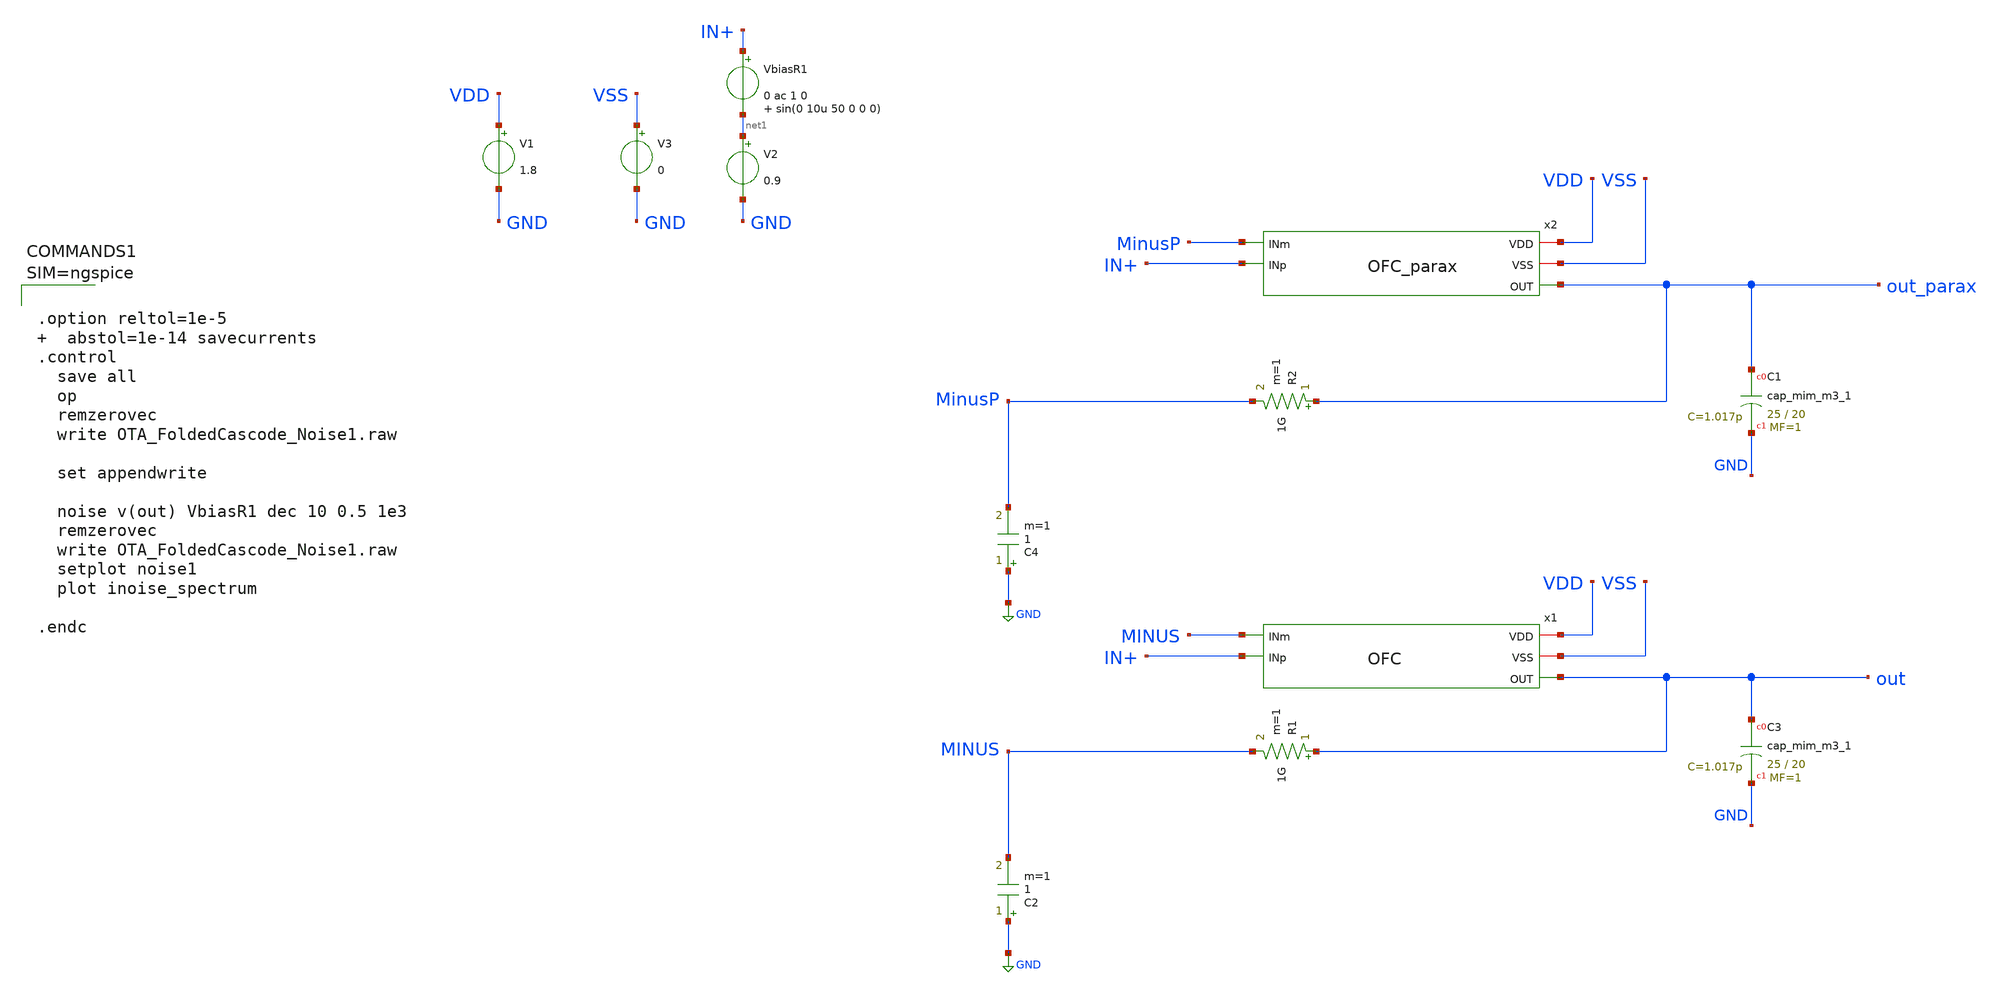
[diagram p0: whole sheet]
** sch_path: tt_um_NE567Mixer28/xschem/OTA_FoldedCascode_Noise1.sch
**.subckt OTA_FoldedCascode_Noise1
VbiasR1 IN+ net1 0 ac 1 0 sin(0 10u 50 0 0 0)
V2 net1 GND 0.9
XC3 out GND sky130_fd_pr__cap_mim_m3_1 W=25 L=20 MF=1 m=1
C2 GND MINUS 1 m=1
R1 out MINUS 1G m=1
V1 VDD GND 1.8
V3 VSS GND 0
x1 VDD VSS out MINUS IN+ OFC
x2 VDD VSS out_parax MinusP IN+ OFC_parax
XC1 out_parax GND sky130_fd_pr__cap_mim_m3_1 W=25 L=20 MF=1 m=1
C4 GND MinusP 1 m=1
R2 out_parax MinusP 1G m=1
**** begin user architecture code



.option reltol=1e-5   abstol=1e-14 savecurrents
.control
  save all
  op
  remzerovec
  write OTA_FoldedCascode_Noise1.raw

  set appendwrite

  noise v(out) VbiasR1 dec 10 0.5 1e3
  remzerovec
  write OTA_FoldedCascode_Noise1.raw
  setplot noise1
  plot inoise_spectrum

.endc



.lib $::SKYWATER_MODELS/sky130.lib.spice tt
**** end user architecture code
**.ends

* expanding   symbol:  OFC.sym # of pins=5
** sym_path: tt_um_NE567Mixer28/xschem/OFC.sym
** sch_path: tt_um_NE567Mixer28/xschem/OFC.sch
.subckt OFC VDD VSS OUT INm INp
*.iopin VDD
*.iopin VSS
*.ipin INp
*.ipin INm
*.opin OUT
XM11 S Vb VDD VDD sky130_fd_pr__pfet_01v8_lvt L=1 W=60 nf=6 ad='int((nf+1)/2) * W/nf * 0.29' as='int((nf+2)/2) * W/nf * 0.29'
+ pd='2*int((nf+1)/2) * (W/nf + 0.29)' ps='2*int((nf+2)/2) * (W/nf + 0.29)' nrd='0.29 / W' nrs='0.29 / W'
+ sa=0 sb=0 sd=0 mult=2 m=2
XM1 D1 INp S S sky130_fd_pr__pfet_01v8_lvt L=10 W=25 nf=2 ad='int((nf+1)/2) * W/nf * 0.29' as='int((nf+2)/2) * W/nf * 0.29'
+ pd='2*int((nf+1)/2) * (W/nf + 0.29)' ps='2*int((nf+2)/2) * (W/nf + 0.29)' nrd='0.29 / W' nrs='0.29 / W'
+ sa=0 sb=0 sd=0 mult=2 m=2
XM2 D2 INm S S sky130_fd_pr__pfet_01v8_lvt L=10 W=25 nf=2 ad='int((nf+1)/2) * W/nf * 0.29' as='int((nf+2)/2) * W/nf * 0.29'
+ pd='2*int((nf+1)/2) * (W/nf + 0.29)' ps='2*int((nf+2)/2) * (W/nf + 0.29)' nrd='0.29 / W' nrs='0.29 / W'
+ sa=0 sb=0 sd=0 mult=2 m=2
XM3 OUT Vc1 D2 VSS sky130_fd_pr__nfet_01v8_lvt L=1 W=4 nf=1 ad='int((nf+1)/2) * W/nf * 0.29' as='int((nf+2)/2) * W/nf * 0.29'
+ pd='2*int((nf+1)/2) * (W/nf + 0.29)' ps='2*int((nf+2)/2) * (W/nf + 0.29)' nrd='0.29 / W' nrs='0.29 / W'
+ sa=0 sb=0 sd=0 mult=1 m=1
XM4 D2 Vc VSS VSS sky130_fd_pr__nfet_01v8_lvt L=1 W=2.8 nf=1 ad='int((nf+1)/2) * W/nf * 0.29' as='int((nf+2)/2) * W/nf * 0.29'
+ pd='2*int((nf+1)/2) * (W/nf + 0.29)' ps='2*int((nf+2)/2) * (W/nf + 0.29)' nrd='0.29 / W' nrs='0.29 / W'
+ sa=0 sb=0 sd=0 mult=1 m=1
XM5 D1 Vc VSS VSS sky130_fd_pr__nfet_01v8_lvt L=1 W=2.8 nf=1 ad='int((nf+1)/2) * W/nf * 0.29' as='int((nf+2)/2) * W/nf * 0.29'
+ pd='2*int((nf+1)/2) * (W/nf + 0.29)' ps='2*int((nf+2)/2) * (W/nf + 0.29)' nrd='0.29 / W' nrs='0.29 / W'
+ sa=0 sb=0 sd=0 mult=1 m=1
XM6 G Vc1 D1 VSS sky130_fd_pr__nfet_01v8_lvt L=1 W=4 nf=1 ad='int((nf+1)/2) * W/nf * 0.29' as='int((nf+2)/2) * W/nf * 0.29'
+ pd='2*int((nf+1)/2) * (W/nf + 0.29)' ps='2*int((nf+2)/2) * (W/nf + 0.29)' nrd='0.29 / W' nrs='0.29 / W'
+ sa=0 sb=0 sd=0 mult=1 m=1
XM7 G Vc2 D9 D9 sky130_fd_pr__pfet_01v8_lvt L=2.23 W=3 nf=1 ad='int((nf+1)/2) * W/nf * 0.29' as='int((nf+2)/2) * W/nf * 0.29'
+ pd='2*int((nf+1)/2) * (W/nf + 0.29)' ps='2*int((nf+2)/2) * (W/nf + 0.29)' nrd='0.29 / W' nrs='0.29 / W'
+ sa=0 sb=0 sd=0 mult=1 m=1
XM9 D9 G VDD VDD sky130_fd_pr__pfet_01v8_lvt L=2.23 W=4 nf=1 ad='int((nf+1)/2) * W/nf * 0.29' as='int((nf+2)/2) * W/nf * 0.29'
+ pd='2*int((nf+1)/2) * (W/nf + 0.29)' ps='2*int((nf+2)/2) * (W/nf + 0.29)' nrd='0.29 / W' nrs='0.29 / W'
+ sa=0 sb=0 sd=0 mult=1 m=1
XM8 D10 G VDD VDD sky130_fd_pr__pfet_01v8_lvt L=2.23 W=4 nf=1 ad='int((nf+1)/2) * W/nf * 0.29' as='int((nf+2)/2) * W/nf * 0.29'
+ pd='2*int((nf+1)/2) * (W/nf + 0.29)' ps='2*int((nf+2)/2) * (W/nf + 0.29)' nrd='0.29 / W' nrs='0.29 / W'
+ sa=0 sb=0 sd=0 mult=1 m=1
XM10 OUT Vc2 D10 D10 sky130_fd_pr__pfet_01v8_lvt L=2.23 W=3 nf=1 ad='int((nf+1)/2) * W/nf * 0.29' as='int((nf+2)/2) * W/nf * 0.29'
+ pd='2*int((nf+1)/2) * (W/nf + 0.29)' ps='2*int((nf+2)/2) * (W/nf + 0.29)' nrd='0.29 / W' nrs='0.29 / W'
+ sa=0 sb=0 sd=0 mult=1 m=1
XR2 Vb VDD VSS sky130_fd_pr__res_xhigh_po_0p35 L=5 mult=1 m=1
XR3 VSS Vb VSS sky130_fd_pr__res_xhigh_po_0p35 L=13.2 mult=1 m=1
XR1 Vc VDD VSS sky130_fd_pr__res_xhigh_po_0p35 L=5 mult=1 m=1
XR4 VSS Vc VSS sky130_fd_pr__res_xhigh_po_0p35 L=3.07 mult=1 m=1
XR5 Vc1 VDD VSS sky130_fd_pr__res_xhigh_po_0p35 L=5 mult=1 m=1
XR6 VSS Vc1 VSS sky130_fd_pr__res_xhigh_po_0p35 L=13.2 mult=1 m=1
XR7 Vc2 VDD VSS sky130_fd_pr__res_xhigh_po_0p35 L=5 mult=1 m=1
XR8 VSS Vc2 VSS sky130_fd_pr__res_xhigh_po_0p35 L=1.6 mult=1 m=1
.ends


* expanding   symbol:  OFC_parax.sym # of pins=5
** sym_path: tt_um_NE567Mixer28/xschem/OFC.sym
.include [file normalize ../mag/OFC.sim.spice]
.GLOBAL GND
.end
